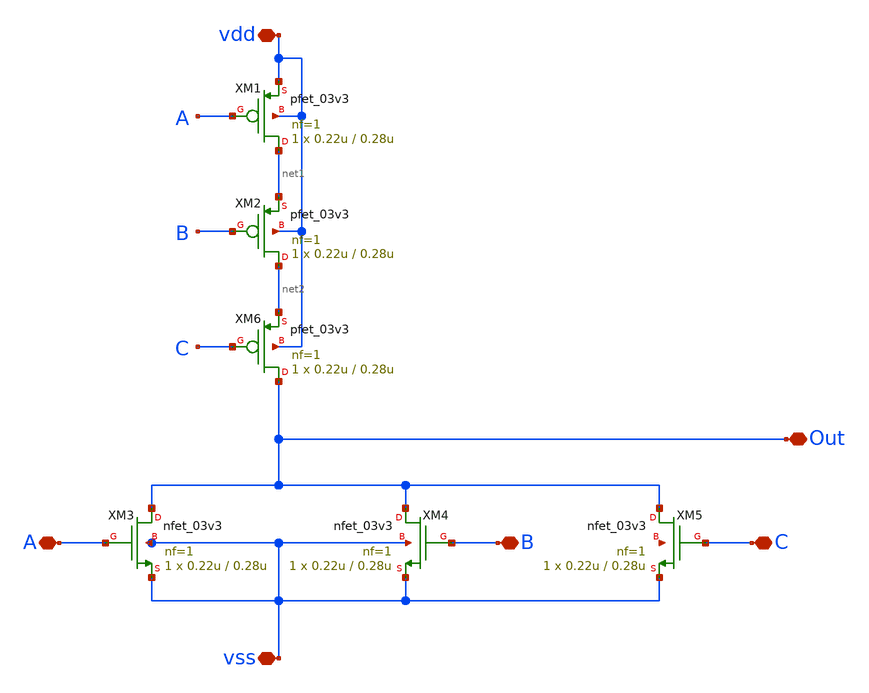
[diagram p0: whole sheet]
** sch_path: designs/libs/adc_singlecycle/nor3.sch
**.subckt nor3 vdd A B vss Out C
*.iopin vdd
*.iopin A
*.iopin B
*.iopin vss
*.iopin Out
*.iopin C
XM1 net1 A vdd vdd pfet_03v3 L=0.28u W=0.22u nf=1 ad='int((nf+1)/2) * W/nf * 0.18u' as='int((nf+2)/2) * W/nf * 0.18u'
+ pd='2*int((nf+1)/2) * (W/nf + 0.18u)' ps='2*int((nf+2)/2) * (W/nf + 0.18u)' nrd='0.18u / W' nrs='0.18u / W'
+ sa=0 sb=0 sd=0 m=1
XM2 net2 B net1 vdd pfet_03v3 L=0.28u W=0.22u nf=1 ad='int((nf+1)/2) * W/nf * 0.18u' as='int((nf+2)/2) * W/nf * 0.18u'
+ pd='2*int((nf+1)/2) * (W/nf + 0.18u)' ps='2*int((nf+2)/2) * (W/nf + 0.18u)' nrd='0.18u / W' nrs='0.18u / W'
+ sa=0 sb=0 sd=0 m=1
XM3 Out A vss vss nfet_03v3 L=0.28u W=0.22u nf=1 ad='int((nf+1)/2) * W/nf * 0.18u' as='int((nf+2)/2) * W/nf * 0.18u'
+ pd='2*int((nf+1)/2) * (W/nf + 0.18u)' ps='2*int((nf+2)/2) * (W/nf + 0.18u)' nrd='0.18u / W' nrs='0.18u / W'
+ sa=0 sb=0 sd=0 m=1
XM4 Out B vss vss nfet_03v3 L=0.28u W=0.22u nf=1 ad='int((nf+1)/2) * W/nf * 0.18u' as='int((nf+2)/2) * W/nf * 0.18u'
+ pd='2*int((nf+1)/2) * (W/nf + 0.18u)' ps='2*int((nf+2)/2) * (W/nf + 0.18u)' nrd='0.18u / W' nrs='0.18u / W'
+ sa=0 sb=0 sd=0 m=1
XM5 Out C vss net3 nfet_03v3 L=0.28u W=0.22u nf=1 ad='int((nf+1)/2) * W/nf * 0.18u' as='int((nf+2)/2) * W/nf * 0.18u'
+ pd='2*int((nf+1)/2) * (W/nf + 0.18u)' ps='2*int((nf+2)/2) * (W/nf + 0.18u)' nrd='0.18u / W' nrs='0.18u / W'
+ sa=0 sb=0 sd=0 m=1
XM6 Out C net2 vdd pfet_03v3 L=0.28u W=0.22u nf=1 ad='int((nf+1)/2) * W/nf * 0.18u' as='int((nf+2)/2) * W/nf * 0.18u'
+ pd='2*int((nf+1)/2) * (W/nf + 0.18u)' ps='2*int((nf+2)/2) * (W/nf + 0.18u)' nrd='0.18u / W' nrs='0.18u / W'
+ sa=0 sb=0 sd=0 m=1
**.ends
.end
